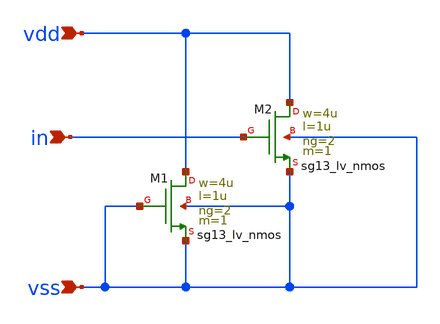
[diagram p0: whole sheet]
** sch_path: Designs/otas/1_schematics/testing_dummies.sch
* Copyright 2024 IHP PDK Authors
**.subckt testing_dummies vss vdd in
*.ipin vss
*.ipin vdd
*.ipin in
XM2 vdd in vss vss sg13_lv_nmos w=4u l=1u ng=2 m=1 mm_ok=1
XM1 vdd vss vss vss sg13_lv_nmos w=4u l=1u ng=2 m=1 mm_ok=1
**.ends
.end
